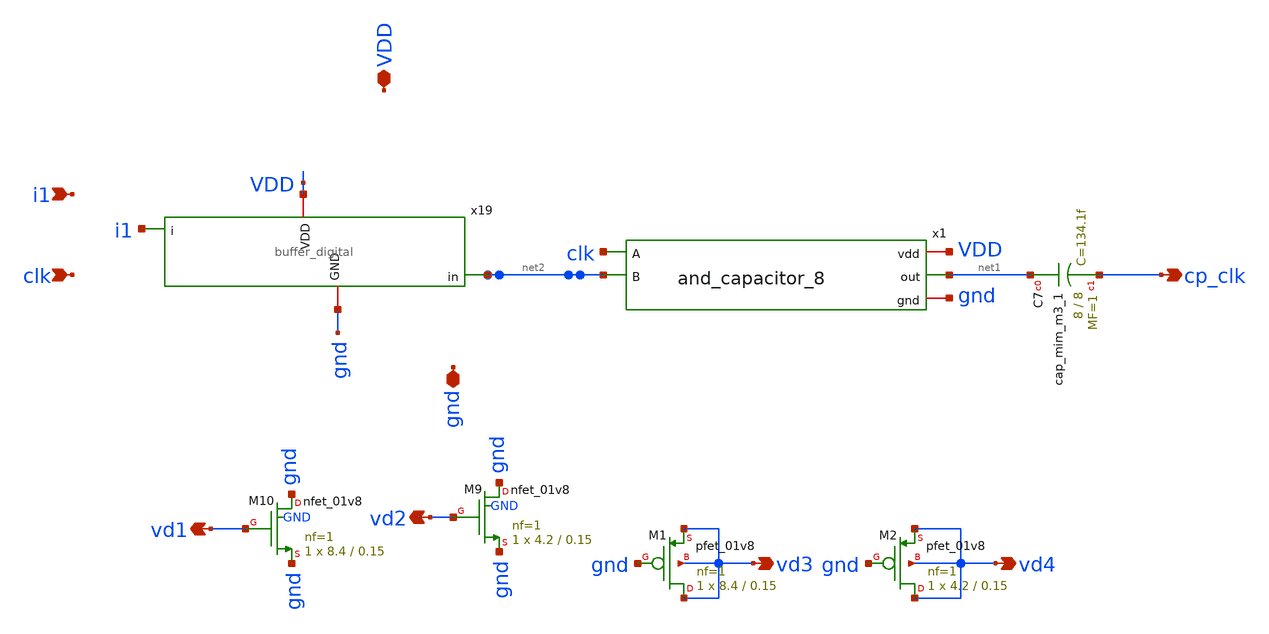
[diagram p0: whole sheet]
** sch_path: xschem/capacitor_8.sch
**.subckt capacitor_8 i1 clk cp_clk VDD gnd vd1 vd2 vd3 vd4
*.ipin i1
*.ipin clk
*.opin cp_clk
*.iopin VDD
*.iopin gnd
*.opin vd1
*.opin vd2
*.opin vd3
*.opin vd4
x19 gnd VDD i1 net2 buffer_digital
x1 VDD net1 clk net2 gnd and_capacitor_8
XM9 gnd vd2 gnd GND sky130_fd_pr__nfet_01v8 L=0.15 W=4.2 nf=1 ad='int((nf+1)/2) * W/nf * 0.29' as='int((nf+2)/2) * W/nf * 0.29'
+ pd='2*int((nf+1)/2) * (W/nf + 0.29)' ps='2*int((nf+2)/2) * (W/nf + 0.29)' nrd='0.29 / W' nrs='0.29 / W'
+ sa=0 sb=0 sd=0 mult=1 m=1
XM10 gnd vd1 gnd GND sky130_fd_pr__nfet_01v8 L=0.15 W=8.4 nf=1 ad='int((nf+1)/2) * W/nf * 0.29' as='int((nf+2)/2) * W/nf * 0.29'
+ pd='2*int((nf+1)/2) * (W/nf + 0.29)' ps='2*int((nf+2)/2) * (W/nf + 0.29)' nrd='0.29 / W' nrs='0.29 / W'
+ sa=0 sb=0 sd=0 mult=1 m=1
XC7 net1 cp_clk sky130_fd_pr__cap_mim_m3_1 W=8 L=8 MF=1 m=1
XM1 vd3 gnd vd3 vd3 sky130_fd_pr__pfet_01v8 L=0.15 W=8.4 nf=1 ad='int((nf+1)/2) * W/nf * 0.29' as='int((nf+2)/2) * W/nf * 0.29'
+ pd='2*int((nf+1)/2) * (W/nf + 0.29)' ps='2*int((nf+2)/2) * (W/nf + 0.29)' nrd='0.29 / W' nrs='0.29 / W'
+ sa=0 sb=0 sd=0 mult=1 m=1
XM2 vd4 gnd vd4 vd4 sky130_fd_pr__pfet_01v8 L=0.15 W=4.2 nf=1 ad='int((nf+1)/2) * W/nf * 0.29' as='int((nf+2)/2) * W/nf * 0.29'
+ pd='2*int((nf+1)/2) * (W/nf + 0.29)' ps='2*int((nf+2)/2) * (W/nf + 0.29)' nrd='0.29 / W' nrs='0.29 / W'
+ sa=0 sb=0 sd=0 mult=1 m=1
**.ends
.end
